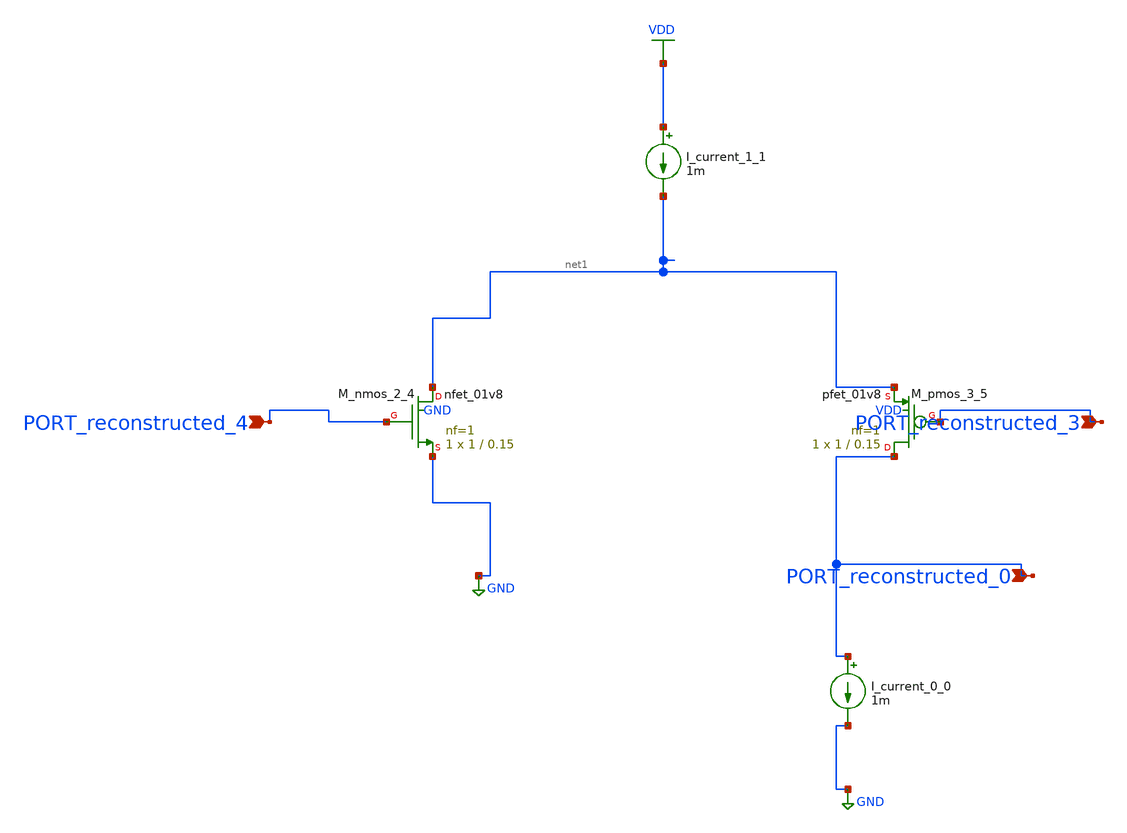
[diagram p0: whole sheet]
** sch_path: schematics/AMSNet/635.sch
**.subckt 635 PORT_reconstructed_0 PORT_reconstructed_3 PORT_reconstructed_4
*.ipin PORT_reconstructed_0
*.ipin PORT_reconstructed_3
*.ipin PORT_reconstructed_4
I_current_0_0 PORT_reconstructed_0 GND 1m
I_current_1_1 VDD net1 1m
XM_nmos_2_4 net1 PORT_reconstructed_4 GND GND sky130_fd_pr__nfet_01v8 L=0.15 W=1 nf=1 ad='int((1 + 1)/2) * 1 / 1 * 0.29'
+ as='int((1 + 2)/2) * 1 / 1 * 0.29' pd='2*int((1 + 1)/2) * (1 / 1 + 0.29)' ps='2*int((1 + 2)/2) * (1 / 1 + 0.29)'
+ nrd='0.29 / 1 ' nrs='0.29 / 1 ' sa=0 sb=0 sd=0 mult=1 m=1
XM_pmos_3_5 PORT_reconstructed_0 PORT_reconstructed_3 net1 VDD sky130_fd_pr__pfet_01v8 L=0.15 W=1 nf=1
+ ad='int((1 + 1)/2) * 1 / 1 * 0.29' as='int((1 + 2)/2) * 1 / 1 * 0.29' pd='2*int((1 + 1)/2) * (1 / 1 + 0.29)'
+ ps='2*int((1 + 2)/2) * (1 / 1 + 0.29)' nrd='0.29 / 1 ' nrs='0.29 / 1 ' sa=0 sb=0 sd=0 mult=1 m=1
**.ends
.GLOBAL GND
.GLOBAL VDD
.end
